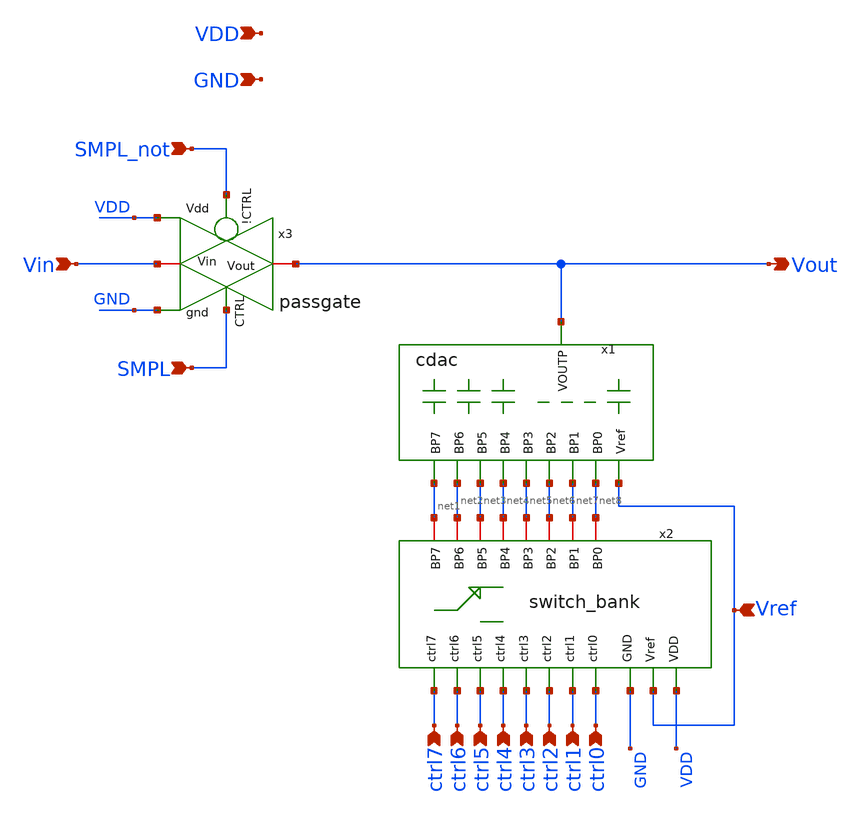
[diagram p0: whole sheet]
** sch_path: 05_mixed_signal/soluzioni/lab01/xschem/cdac_complete.sch
**.subckt cdac_complete VDD GND Vref Vin Vout SMPL SMPL_not ctrl7 ctrl6 ctrl5 ctrl4 ctrl3 ctrl2
*+ ctrl1 ctrl0
*.ipin VDD
*.ipin GND
*.ipin Vref
*.ipin Vin
*.opin Vout
*.ipin SMPL
*.ipin SMPL_not
*.ipin ctrl7
*.ipin ctrl6
*.ipin ctrl5
*.ipin ctrl4
*.ipin ctrl3
*.ipin ctrl2
*.ipin ctrl1
*.ipin ctrl0
x1 Vout Vref net5 net6 net3 net4 net7 net2 net1 net8 cdac
x2 net8 net3 net6 net5 net1 net4 net7 net2 VDD ctrl5 ctrl6 ctrl7 ctrl1 ctrl4 ctrl2 ctrl3 ctrl0 Vref
+ GND switch_bank
x3 Vin GND SMPL_not SMPL VDD Vout passgate
**.ends
.end
